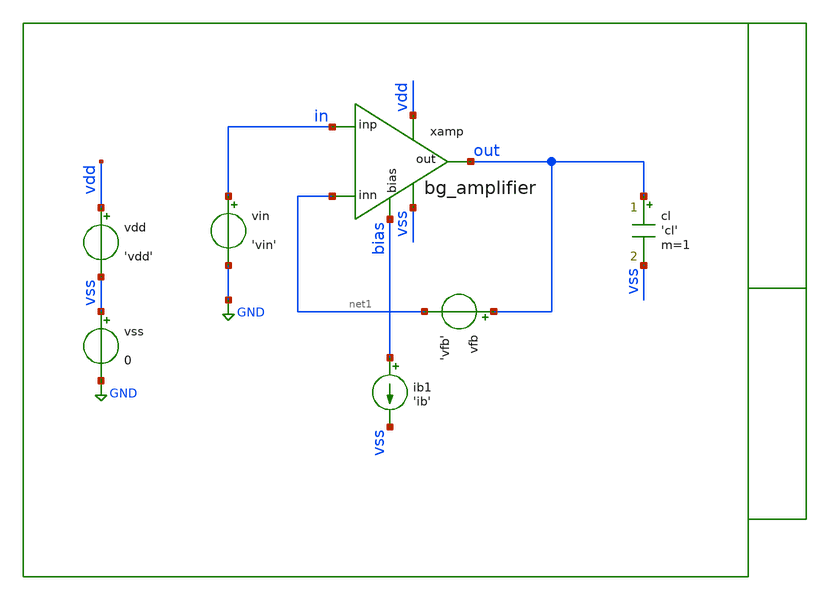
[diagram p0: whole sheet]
** sch_path: xschem/tb/bandgap_cm/bg_amplifier/op_bg_amplifier.sch
**.subckt op_bg_amplifier
cl out vss 'cl' m=1
vin in GND 'vin'
vdd vdd vss 'vdd'
vss vss GND 0
xamp vdd out in net1 vss bias bg_amplifier
vfb out net1 'vfb'
ib1 bias vss 'ib'
**** begin user architecture code

* Control

.param vdd=3.0

* emulate bandgap setup
.param vfb=1.4
.param vin=0.7
.param ib=1u
.param cl=1p


.control
save all
op

let gds_xmb1 = @m.xamp.xmb1.m0[gds]
let gds_xmb2 = @m.xamp.xmb2.m0[gds]
let gds_xmb3 = @m.xamp.xmb3.m0[gds]
let gds_xmb4 = @m.xamp.xmb4.m0[gds]
let gds_xmb5 = @m.xamp.xmb5.m0[gds]
let gds_xmc1 = @m.xamp.xmc1.m0[gds]
let gds_xmc2 = @m.xamp.xmc2.m0[gds]
let gds_xmc3 = @m.xamp.xmc3.m0[gds]
let gds_xmc4 = @m.xamp.xmc4.m0[gds]
let gds_xmc5 = @m.xamp.xmc5.m0[gds]
let gds_xmc6 = @m.xamp.xmc6.m0[gds]
let gds_xmc7 = @m.xamp.xmc7.m0[gds]
let gds_xmc8 = @m.xamp.xmc8.m0[gds]
let gds_xmd1 = @m.xamp.xmd1.m0[gds]
let gds_xmd2 = @m.xamp.xmd2.m0[gds]
let gds_xmt1 = @m.xamp.xmt1.m0[gds]
let gm_xmb1 = @m.xamp.xmb1.m0[gm]
let gm_xmb2 = @m.xamp.xmb2.m0[gm]
let gm_xmb3 = @m.xamp.xmb3.m0[gm]
let gm_xmb4 = @m.xamp.xmb4.m0[gm]
let gm_xmb5 = @m.xamp.xmb5.m0[gm]
let gm_xmc1 = @m.xamp.xmc1.m0[gm]
let gm_xmc2 = @m.xamp.xmc2.m0[gm]
let gm_xmc3 = @m.xamp.xmc3.m0[gm]
let gm_xmc4 = @m.xamp.xmc4.m0[gm]
let gm_xmc5 = @m.xamp.xmc5.m0[gm]
let gm_xmc6 = @m.xamp.xmc6.m0[gm]
let gm_xmc7 = @m.xamp.xmc7.m0[gm]
let gm_xmc8 = @m.xamp.xmc8.m0[gm]
let gm_xmd1 = @m.xamp.xmd1.m0[gm]
let gm_xmd2 = @m.xamp.xmd2.m0[gm]
let gm_xmt1 = @m.xamp.xmt1.m0[gm]
let id_xmb1 = @m.xamp.xmb1.m0[id]
let id_xmb2 = @m.xamp.xmb2.m0[id]
let id_xmb3 = @m.xamp.xmb3.m0[id]
let id_xmb4 = @m.xamp.xmb4.m0[id]
let id_xmb5 = @m.xamp.xmb5.m0[id]
let id_xmc1 = @m.xamp.xmc1.m0[id]
let id_xmc2 = @m.xamp.xmc2.m0[id]
let id_xmc3 = @m.xamp.xmc3.m0[id]
let id_xmc4 = @m.xamp.xmc4.m0[id]
let id_xmc5 = @m.xamp.xmc5.m0[id]
let id_xmc6 = @m.xamp.xmc6.m0[id]
let id_xmc7 = @m.xamp.xmc7.m0[id]
let id_xmc8 = @m.xamp.xmc8.m0[id]
let id_xmd1 = @m.xamp.xmd1.m0[id]
let id_xmd2 = @m.xamp.xmd2.m0[id]
let id_xmt1 = @m.xamp.xmt1.m0[id]
let vds_xmb1 = @m.xamp.xmb1.m0[vds]
let vds_xmb2 = @m.xamp.xmb2.m0[vds]
let vds_xmb3 = @m.xamp.xmb3.m0[vds]
let vds_xmb4 = @m.xamp.xmb4.m0[vds]
let vds_xmb5 = @m.xamp.xmb5.m0[vds]
let vds_xmc1 = @m.xamp.xmc1.m0[vds]
let vds_xmc2 = @m.xamp.xmc2.m0[vds]
let vds_xmc3 = @m.xamp.xmc3.m0[vds]
let vds_xmc4 = @m.xamp.xmc4.m0[vds]
let vds_xmc5 = @m.xamp.xmc5.m0[vds]
let vds_xmc6 = @m.xamp.xmc6.m0[vds]
let vds_xmc7 = @m.xamp.xmc7.m0[vds]
let vds_xmc8 = @m.xamp.xmc8.m0[vds]
let vds_xmd1 = @m.xamp.xmd1.m0[vds]
let vds_xmd2 = @m.xamp.xmd2.m0[vds]
let vds_xmt1 = @m.xamp.xmt1.m0[vds]
let vdsat_xmb1 = @m.xamp.xmb1.m0[vdsat]
let vdsat_xmb2 = @m.xamp.xmb2.m0[vdsat]
let vdsat_xmb3 = @m.xamp.xmb3.m0[vdsat]
let vdsat_xmb4 = @m.xamp.xmb4.m0[vdsat]
let vdsat_xmb5 = @m.xamp.xmb5.m0[vdsat]
let vdsat_xmc1 = @m.xamp.xmc1.m0[vdsat]
let vdsat_xmc2 = @m.xamp.xmc2.m0[vdsat]
let vdsat_xmc3 = @m.xamp.xmc3.m0[vdsat]
let vdsat_xmc4 = @m.xamp.xmc4.m0[vdsat]
let vdsat_xmc5 = @m.xamp.xmc5.m0[vdsat]
let vdsat_xmc6 = @m.xamp.xmc6.m0[vdsat]
let vdsat_xmc7 = @m.xamp.xmc7.m0[vdsat]
let vdsat_xmc8 = @m.xamp.xmc8.m0[vdsat]
let vdsat_xmd1 = @m.xamp.xmd1.m0[vdsat]
let vdsat_xmd2 = @m.xamp.xmd2.m0[vdsat]
let vdsat_xmt1 = @m.xamp.xmt1.m0[vdsat]
let vgs_xmb1 = @m.xamp.xmb1.m0[vgs]
let vgs_xmb2 = @m.xamp.xmb2.m0[vgs]
let vgs_xmb3 = @m.xamp.xmb3.m0[vgs]
let vgs_xmb4 = @m.xamp.xmb4.m0[vgs]
let vgs_xmb5 = @m.xamp.xmb5.m0[vgs]
let vgs_xmc1 = @m.xamp.xmc1.m0[vgs]
let vgs_xmc2 = @m.xamp.xmc2.m0[vgs]
let vgs_xmc3 = @m.xamp.xmc3.m0[vgs]
let vgs_xmc4 = @m.xamp.xmc4.m0[vgs]
let vgs_xmc5 = @m.xamp.xmc5.m0[vgs]
let vgs_xmc6 = @m.xamp.xmc6.m0[vgs]
let vgs_xmc7 = @m.xamp.xmc7.m0[vgs]
let vgs_xmc8 = @m.xamp.xmc8.m0[vgs]
let vgs_xmd1 = @m.xamp.xmd1.m0[vgs]
let vgs_xmd2 = @m.xamp.xmd2.m0[vgs]
let vgs_xmt1 = @m.xamp.xmt1.m0[vgs]
let vth_xmb1 = @m.xamp.xmb1.m0[vth]
let vth_xmb2 = @m.xamp.xmb2.m0[vth]
let vth_xmb3 = @m.xamp.xmb3.m0[vth]
let vth_xmb4 = @m.xamp.xmb4.m0[vth]
let vth_xmb5 = @m.xamp.xmb5.m0[vth]
let vth_xmc1 = @m.xamp.xmc1.m0[vth]
let vth_xmc2 = @m.xamp.xmc2.m0[vth]
let vth_xmc3 = @m.xamp.xmc3.m0[vth]
let vth_xmc4 = @m.xamp.xmc4.m0[vth]
let vth_xmc5 = @m.xamp.xmc5.m0[vth]
let vth_xmc6 = @m.xamp.xmc6.m0[vth]
let vth_xmc7 = @m.xamp.xmc7.m0[vth]
let vth_xmc8 = @m.xamp.xmc8.m0[vth]
let vth_xmd1 = @m.xamp.xmd1.m0[vth]
let vth_xmd2 = @m.xamp.xmd2.m0[vth]
let vth_xmt1 = @m.xamp.xmt1.m0[vth]

let vov_xmb1 = vgs_xmb1-vth_xmb1
let vov_xmb2 = vgs_xmb2-vth_xmb2
let vov_xmb3 = vgs_xmb3-vth_xmb3
let vov_xmb4 = vgs_xmb4-vth_xmb4
let vov_xmb5 = vgs_xmb5-vth_xmb5
let vov_xmc1 = vgs_xmc1-vth_xmc1
let vov_xmc2 = vgs_xmc2-vth_xmc2
let vov_xmc3 = vgs_xmc3-vth_xmc3
let vov_xmc4 = vgs_xmc4-vth_xmc4
let vov_xmc5 = vgs_xmc5-vth_xmc5
let vov_xmc6 = vgs_xmc6-vth_xmc6
let vov_xmc7 = vgs_xmc7-vth_xmc7
let vov_xmc8 = vgs_xmc8-vth_xmc8
let vov_xmd1 = vgs_xmd1-vth_xmd1
let vov_xmd2 = vgs_xmd2-vth_xmd2
let vov_xmt1 = vgs_xmt1-vth_xmt1

let vsat_xmb1 = vds_xmb1-vdsat_xmb1
let vsat_xmb2 = vds_xmb2-vdsat_xmb2
let vsat_xmb3 = vds_xmb3-vdsat_xmb3
let vsat_xmb4 = vds_xmb4-vdsat_xmb4
let vsat_xmb5 = vds_xmb5-vdsat_xmb5
let vsat_xmc1 = vds_xmc1-vdsat_xmc1
let vsat_xmc2 = vds_xmc2-vdsat_xmc2
let vsat_xmc3 = vds_xmc3-vdsat_xmc3
let vsat_xmc4 = vds_xmc4-vdsat_xmc4
let vsat_xmc5 = vds_xmc5-vdsat_xmc5
let vsat_xmc6 = vds_xmc6-vdsat_xmc6
let vsat_xmc7 = vds_xmc7-vdsat_xmc7
let vsat_xmc8 = vds_xmc8-vdsat_xmc8
let vsat_xmd1 = vds_xmd1-vdsat_xmd1
let vsat_xmd2 = vds_xmd2-vdsat_xmd2
let vsat_xmt1 = vds_xmt1-vdsat_xmt1



print gds_xmb1
print gds_xmb2
print gds_xmb3
print gds_xmb4
print gds_xmb5
print gds_xmc1
print gds_xmc2
print gds_xmc3
print gds_xmc4
print gds_xmc5
print gds_xmc6
print gds_xmc7
print gds_xmc8
print gds_xmd1
print gds_xmd2
print gds_xmt1
print gm_xmb1
print gm_xmb2
print gm_xmb3
print gm_xmb4
print gm_xmb5
print gm_xmc1
print gm_xmc2
print gm_xmc3
print gm_xmc4
print gm_xmc5
print gm_xmc6
print gm_xmc7
print gm_xmc8
print gm_xmd1
print gm_xmd2
print gm_xmt1
print id_xmb1
print id_xmb2
print id_xmb3
print id_xmb4
print id_xmb5
print id_xmc1
print id_xmc2
print id_xmc3
print id_xmc4
print id_xmc5
print id_xmc6
print id_xmc7
print id_xmc8
print id_xmd1
print id_xmd2
print id_xmt1
print vds_xmb1
print vds_xmb2
print vds_xmb3
print vds_xmb4
print vds_xmb5
print vds_xmc1
print vds_xmc2
print vds_xmc3
print vds_xmc4
print vds_xmc5
print vds_xmc6
print vds_xmc7
print vds_xmc8
print vds_xmd1
print vds_xmd2
print vds_xmt1
print vdsat_xmb1
print vdsat_xmb2
print vdsat_xmb3
print vdsat_xmb4
print vdsat_xmb5
print vdsat_xmc1
print vdsat_xmc2
print vdsat_xmc3
print vdsat_xmc4
print vdsat_xmc5
print vdsat_xmc6
print vdsat_xmc7
print vdsat_xmc8
print vdsat_xmd1
print vdsat_xmd2
print vdsat_xmt1
print vgs_xmb1
print vgs_xmb2
print vgs_xmb3
print vgs_xmb4
print vgs_xmb5
print vgs_xmc1
print vgs_xmc2
print vgs_xmc3
print vgs_xmc4
print vgs_xmc5
print vgs_xmc6
print vgs_xmc7
print vgs_xmc8
print vgs_xmd1
print vgs_xmd2
print vgs_xmt1
print vth_xmb1
print vth_xmb2
print vth_xmb3
print vth_xmb4
print vth_xmb5
print vth_xmc1
print vth_xmc2
print vth_xmc3
print vth_xmc4
print vth_xmc5
print vth_xmc6
print vth_xmc7
print vth_xmc8
print vth_xmd1
print vth_xmd2
print vth_xmt1
print vov_xmb1
print vov_xmb2
print vov_xmb3
print vov_xmb4
print vov_xmb5
print vov_xmc1
print vov_xmc2
print vov_xmc3
print vov_xmc4
print vov_xmc5
print vov_xmc6
print vov_xmc7
print vov_xmc8
print vov_xmd1
print vov_xmd2
print vov_xmt1
print vsat_xmb1
print vsat_xmb2
print vsat_xmb3
print vsat_xmb4
print vsat_xmb5
print vsat_xmc1
print vsat_xmc2
print vsat_xmc3
print vsat_xmc4
print vsat_xmc5
print vsat_xmc6
print vsat_xmc7
print vsat_xmc8
print vsat_xmd1
print vsat_xmd2
print vsat_xmt1


* nodes
let mirr = xamp.mirr
let vbp1 = xamp.vbn1
let vbp2 = xamp.vbn2
let vbn1 = xamp.vbp1
let vcm  = xamp.vcm
let vop  = xamp.vop
let von  = xamp.von
let vda  = xamp.vda
let vdb  = xamp.vdb

print in
print out
print bias
print mirr
print vbp1
print vbp2
print vbn1
print vcm
print vop
print von
print vda
print vdb

write op_bg_amplifier.raw

.endc


 * Model Corners

.include $::CORNERS/ngspice/tt.spice
*.include $::CORNERS/ngspice/ff.spice
*.include $::CORNERS/ngspice/ss.spice
*.include $::CORNERS/ngspice/sf.spice
*.include $::CORNERS/ngspice/fs.spice

 * extract

* pex
*.include $::DESIGN_PATH/sch/bandgap_cm/bg_amplifier/bg_amplifier.pex.spice

**** end user architecture code
**.ends

* expanding   symbol:  sch/bandgap_cm/bg_amplifier/bg_amplifier.sym # of pins=6
** sym_path: xschem/sch/bandgap_cm/bg_amplifier/bg_amplifier.sym
** sch_path: xschem/sch/bandgap_cm/bg_amplifier/bg_amplifier.sch
.subckt bg_amplifier vdd out inp inn vss bias
*.ipin inn
*.ipin inp
*.opin out
*.iopin bias
*.iopin vdd
*.iopin vss
XMB5 vbn1 vbn1 vss vss nfet_06v0 L=2u W=16u nf=2 ad='int((nf+1)/2) * W/nf * 0.18u' as='int((nf+2)/2) * W/nf * 0.18u'
+ pd='2*int((nf+1)/2) * (W/nf + 0.18u)' ps='2*int((nf+2)/2) * (W/nf + 0.18u)' nrd='0.18u / W' nrs='0.18u / W'
+ sa=0 sb=0 sd=0 m=4 par=4
XMC1 von vbn1 vss vss nfet_06v0 L=2u W=16u nf=2 ad='int((nf+1)/2) * W/nf * 0.18u' as='int((nf+2)/2) * W/nf * 0.18u'
+ pd='2*int((nf+1)/2) * (W/nf + 0.18u)' ps='2*int((nf+2)/2) * (W/nf + 0.18u)' nrd='0.18u / W' nrs='0.18u / W'
+ sa=0 sb=0 sd=0 m=10 par=10
XMC2 vop vbn1 vss vss nfet_06v0 L=2u W=16u nf=2 ad='int((nf+1)/2) * W/nf * 0.18u' as='int((nf+2)/2) * W/nf * 0.18u'
+ pd='2*int((nf+1)/2) * (W/nf + 0.18u)' ps='2*int((nf+2)/2) * (W/nf + 0.18u)' nrd='0.18u / W' nrs='0.18u / W'
+ sa=0 sb=0 sd=0 m=10 par=10
XMC3 mirr vbn2 von vss nfet_06v0 L=2u W=16u nf=2 ad='int((nf+1)/2) * W/nf * 0.18u' as='int((nf+2)/2) * W/nf * 0.18u'
+ pd='2*int((nf+1)/2) * (W/nf + 0.18u)' ps='2*int((nf+2)/2) * (W/nf + 0.18u)' nrd='0.18u / W' nrs='0.18u / W'
+ sa=0 sb=0 sd=0 m=4 par=4
XMC4 out vbn2 vop vss nfet_06v0 L=2u W=16u nf=2 ad='int((nf+1)/2) * W/nf * 0.18u' as='int((nf+2)/2) * W/nf * 0.18u'
+ pd='2*int((nf+1)/2) * (W/nf + 0.18u)' ps='2*int((nf+2)/2) * (W/nf + 0.18u)' nrd='0.18u / W' nrs='0.18u / W'
+ sa=0 sb=0 sd=0 m=4 par=4
XMB3 bias bias vbp1 vdd pfet_06v0 L=2u W=16u nf=2 ad='int((nf+1)/2) * W/nf * 0.18u' as='int((nf+2)/2) * W/nf * 0.18u'
+ pd='2*int((nf+1)/2) * (W/nf + 0.18u)' ps='2*int((nf+2)/2) * (W/nf + 0.18u)' nrd='0.18u / W' nrs='0.18u / W'
+ sa=0 sb=0 sd=0 m=2 par=2
XMB1 vbp1 vbp1 vdd vdd pfet_06v0 L=2u W=16u nf=2 ad='int((nf+1)/2) * W/nf * 0.18u' as='int((nf+2)/2) * W/nf * 0.18u'
+ pd='2*int((nf+1)/2) * (W/nf + 0.18u)' ps='2*int((nf+2)/2) * (W/nf + 0.18u)' nrd='0.18u / W' nrs='0.18u / W'
+ sa=0 sb=0 sd=0 m=4 par=4
XMB2 vbn2 vbp1 vdd vdd pfet_06v0 L=2u W=16u nf=2 ad='int((nf+1)/2) * W/nf * 0.18u' as='int((nf+2)/2) * W/nf * 0.18u'
+ pd='2*int((nf+1)/2) * (W/nf + 0.18u)' ps='2*int((nf+2)/2) * (W/nf + 0.18u)' nrd='0.18u / W' nrs='0.18u / W'
+ sa=0 sb=0 sd=0 m=4 par=4
XMT1 vcm vbp1 vdd vdd pfet_06v0 L=2u W=16u nf=2 ad='int((nf+1)/2) * W/nf * 0.18u' as='int((nf+2)/2) * W/nf * 0.18u'
+ pd='2*int((nf+1)/2) * (W/nf + 0.18u)' ps='2*int((nf+2)/2) * (W/nf + 0.18u)' nrd='0.18u / W' nrs='0.18u / W'
+ sa=0 sb=0 sd=0 m=8 par=8
XMD1 von inp vcm vdd pfet_06v0 L=4u W=16u nf=2 ad='int((nf+1)/2) * W/nf * 0.18u' as='int((nf+2)/2) * W/nf * 0.18u'
+ pd='2*int((nf+1)/2) * (W/nf + 0.18u)' ps='2*int((nf+2)/2) * (W/nf + 0.18u)' nrd='0.18u / W' nrs='0.18u / W'
+ sa=0 sb=0 sd=0 m=4 par=4
XMD2 vop inn vcm vdd pfet_06v0 L=4u W=16u nf=2 ad='int((nf+1)/2) * W/nf * 0.18u' as='int((nf+2)/2) * W/nf * 0.18u'
+ pd='2*int((nf+1)/2) * (W/nf + 0.18u)' ps='2*int((nf+2)/2) * (W/nf + 0.18u)' nrd='0.18u / W' nrs='0.18u / W'
+ sa=0 sb=0 sd=0 m=4 par=4
XMC7 vda mirr vdd vdd pfet_06v0 L=2u W=16u nf=2 ad='int((nf+1)/2) * W/nf * 0.18u' as='int((nf+2)/2) * W/nf * 0.18u'
+ pd='2*int((nf+1)/2) * (W/nf + 0.18u)' ps='2*int((nf+2)/2) * (W/nf + 0.18u)' nrd='0.18u / W' nrs='0.18u / W'
+ sa=0 sb=0 sd=0 m=2 par=2
XMC8 vdb mirr vdd vdd pfet_06v0 L=2u W=16u nf=2 ad='int((nf+1)/2) * W/nf * 0.18u' as='int((nf+2)/2) * W/nf * 0.18u'
+ pd='2*int((nf+1)/2) * (W/nf + 0.18u)' ps='2*int((nf+2)/2) * (W/nf + 0.18u)' nrd='0.18u / W' nrs='0.18u / W'
+ sa=0 sb=0 sd=0 m=2 par=2
XMC5 mirr bias vda vdd pfet_06v0 L=2u W=16u nf=2 ad='int((nf+1)/2) * W/nf * 0.18u' as='int((nf+2)/2) * W/nf * 0.18u'
+ pd='2*int((nf+1)/2) * (W/nf + 0.18u)' ps='2*int((nf+2)/2) * (W/nf + 0.18u)' nrd='0.18u / W' nrs='0.18u / W'
+ sa=0 sb=0 sd=0 m=4 par=4
XMC6 out bias vdb vdd pfet_06v0 L=2u W=16u nf=2 ad='int((nf+1)/2) * W/nf * 0.18u' as='int((nf+2)/2) * W/nf * 0.18u'
+ pd='2*int((nf+1)/2) * (W/nf + 0.18u)' ps='2*int((nf+2)/2) * (W/nf + 0.18u)' nrd='0.18u / W' nrs='0.18u / W'
+ sa=0 sb=0 sd=0 m=4 par=4
XMB4 vbn2 vbn2 vbn1 vss nfet_06v0 L=2u W=16u nf=2 ad='int((nf+1)/2) * W/nf * 0.18u' as='int((nf+2)/2) * W/nf * 0.18u'
+ pd='2*int((nf+1)/2) * (W/nf + 0.18u)' ps='2*int((nf+2)/2) * (W/nf + 0.18u)' nrd='0.18u / W' nrs='0.18u / W'
+ sa=0 sb=0 sd=0 m=4 par=4
XMDUM1 vdd vdd vdd vdd pfet_06v0 L=2u W=16u nf=2 ad='int((nf+1)/2) * W/nf * 0.18u' as='int((nf+2)/2) * W/nf * 0.18u'
+ pd='2*int((nf+1)/2) * (W/nf + 0.18u)' ps='2*int((nf+2)/2) * (W/nf + 0.18u)' nrd='0.18u / W' nrs='0.18u / W'
+ sa=0 sb=0 sd=0 m=4 par=4
XMDUM2 vdd vdd vdd vdd pfet_06v0 L=2u W=16u nf=2 ad='int((nf+1)/2) * W/nf * 0.18u' as='int((nf+2)/2) * W/nf * 0.18u'
+ pd='2*int((nf+1)/2) * (W/nf + 0.18u)' ps='2*int((nf+2)/2) * (W/nf + 0.18u)' nrd='0.18u / W' nrs='0.18u / W'
+ sa=0 sb=0 sd=0 m=4 par=4
XMDUM3 vdd vdd vdd vdd pfet_06v0 L=2u W=16u nf=2 ad='int((nf+1)/2) * W/nf * 0.18u' as='int((nf+2)/2) * W/nf * 0.18u'
+ pd='2*int((nf+1)/2) * (W/nf + 0.18u)' ps='2*int((nf+2)/2) * (W/nf + 0.18u)' nrd='0.18u / W' nrs='0.18u / W'
+ sa=0 sb=0 sd=0 m=2 par=2
XMDUM4 vss vss vss vss nfet_06v0 L=2u W=16u nf=2 ad='int((nf+1)/2) * W/nf * 0.18u' as='int((nf+2)/2) * W/nf * 0.18u'
+ pd='2*int((nf+1)/2) * (W/nf + 0.18u)' ps='2*int((nf+2)/2) * (W/nf + 0.18u)' nrd='0.18u / W' nrs='0.18u / W'
+ sa=0 sb=0 sd=0 m=2 par=2
XMDUM5 vss vss vss vss nfet_06v0 L=2u W=16u nf=2 ad='int((nf+1)/2) * W/nf * 0.18u' as='int((nf+2)/2) * W/nf * 0.18u'
+ pd='2*int((nf+1)/2) * (W/nf + 0.18u)' ps='2*int((nf+2)/2) * (W/nf + 0.18u)' nrd='0.18u / W' nrs='0.18u / W'
+ sa=0 sb=0 sd=0 m=2 par=2
XMDUM6 vdd vdd vdd vdd pfet_06v0 L=4u W=16u nf=2 ad='int((nf+1)/2) * W/nf * 0.18u' as='int((nf+2)/2) * W/nf * 0.18u'
+ pd='2*int((nf+1)/2) * (W/nf + 0.18u)' ps='2*int((nf+2)/2) * (W/nf + 0.18u)' nrd='0.18u / W' nrs='0.18u / W'
+ sa=0 sb=0 sd=0 m=16 par=16
.ends

.GLOBAL GND
.end
